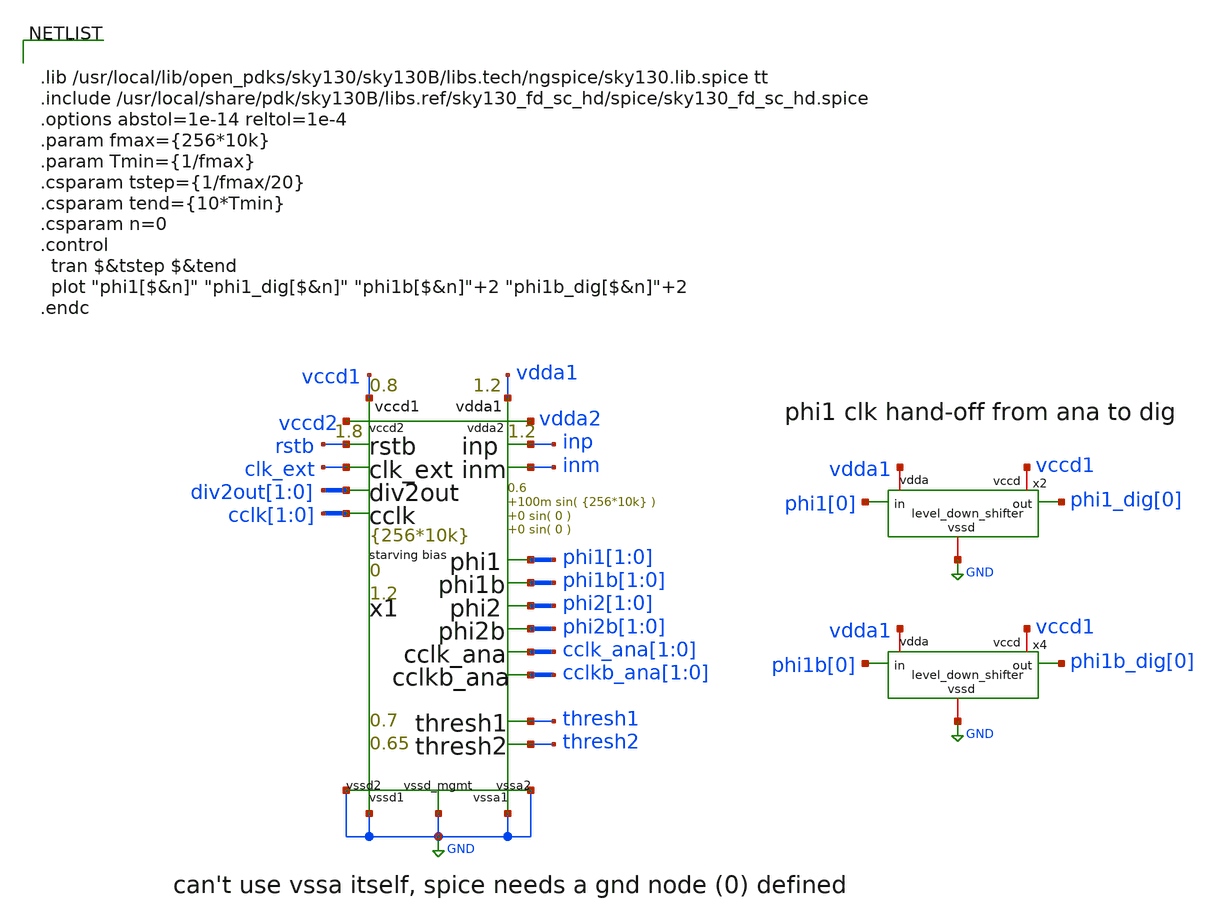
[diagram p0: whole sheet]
** sch_path: xschem/test_bench/level_down_shifter_phi_tb.sch
**.subckt level_down_shifter_phi_tb
x2 vdda1 vccd1 phi1[0] phi1_dig[0] GND level_down_shifter
x4 vdda1 vccd1 phi1b[0] phi1b_dig[0] GND level_down_shifter
x1 thresh1 thresh2 inp inm clk_ext rstb phi1[1] phi1[0] phi1b[1] phi1b[0] phi2[1] phi2[0] phi2b[1] phi2b[0]
+ cclk_ana[1] cclk_ana[0] cclkb_ana[1] cclkb_ana[0] div2out[1] div2out[0] cclk[1] cclk[0] vdda1 vccd1 vccd2
+ vdda2 GND GND GND GND GND risc_signals p_vdda1=1.2 p_vdda2=1.2 p_vccd1=0.8 p_vccd2=1.8 p_vccd_mgmt=1.8
+ p_fclk={256*10k} p_duty_cycle=0.5 p_rstb_delay={1.5/p_fclk} p_rstb_tr=5n p_thresh1=0.7 p_thresh2=0.65
+ p_vpb=0 p_vnb=1.2 p_vcm=0.6 p_amp1=100m p_f1={256*10k} p_amp2=0 p_f2=0 p_amp3=0 p_f3=0
**** begin user architecture code


.lib /usr/local/lib/open_pdks/sky130/sky130B/libs.tech/ngspice/sky130.lib.spice tt
.include /usr/local/share/pdk/sky130B/libs.ref/sky130_fd_sc_hd/spice/sky130_fd_sc_hd.spice
.options abstol=1e-14 reltol=1e-4
.param fmax={256*10k}
.param Tmin={1/fmax}
.csparam tstep={1/fmax/20}
.csparam tend={10*Tmin}
.csparam n=0
.control
  tran $&tstep $&tend
  plot "phi1[$&n]" "phi1_dig[$&n]" "phi1b[$&n]"+2 "phi1b_dig[$&n]"+2
.endc


**** end user architecture code
**.ends
.GLOBAL GND
.end
